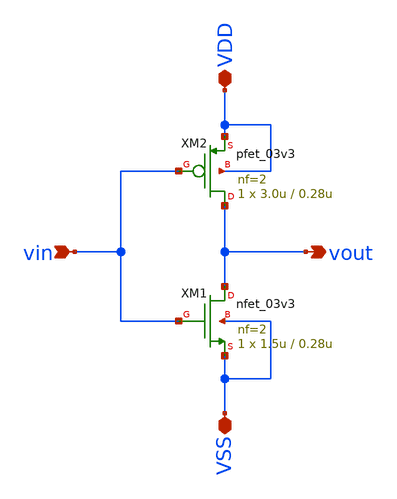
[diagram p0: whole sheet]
** sch_path: designs/libs/core_analog/inv_x3/inv_x3.sch
**.subckt inv_x3 VDD VSS vin vout
*.iopin VDD
*.iopin VSS
*.ipin vin
*.opin vout
XM1 vout vin VSS VSS nfet_03v3 L=0.28u W=1.5u nf=2 ad='int((nf+1)/2) * W/nf * 0.18u' as='int((nf+2)/2) * W/nf * 0.18u'
+ pd='2*int((nf+1)/2) * (W/nf + 0.18u)' ps='2*int((nf+2)/2) * (W/nf + 0.18u)' nrd='0.18u / W' nrs='0.18u / W'
+ sa=0 sb=0 sd=0 m=1
XM2 vout vin VDD VDD pfet_03v3 L=0.28u W=3.0u nf=2 ad='int((nf+1)/2) * W/nf * 0.18u' as='int((nf+2)/2) * W/nf * 0.18u'
+ pd='2*int((nf+1)/2) * (W/nf + 0.18u)' ps='2*int((nf+2)/2) * (W/nf + 0.18u)' nrd='0.18u / W' nrs='0.18u / W'
+ sa=0 sb=0 sd=0 m=1
**.ends
.end
